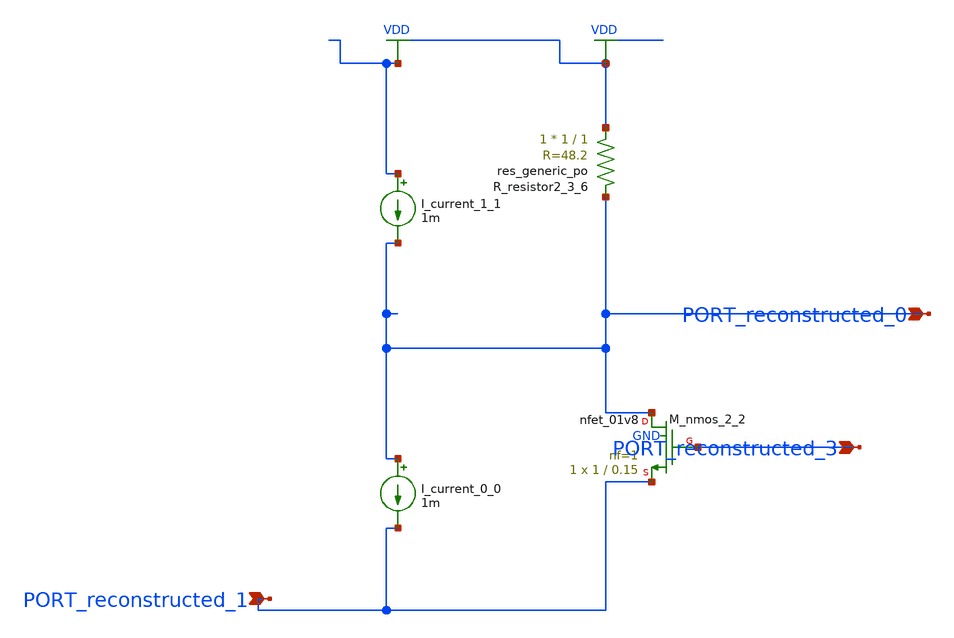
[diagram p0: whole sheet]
** sch_path: schematics/AMSNet/469.sch
**.subckt 469 PORT_reconstructed_3 PORT_reconstructed_1 PORT_reconstructed_0
*.ipin PORT_reconstructed_3
*.ipin PORT_reconstructed_1
*.ipin PORT_reconstructed_0
I_current_0_0 PORT_reconstructed_0 PORT_reconstructed_1 1m
I_current_1_1 VDD PORT_reconstructed_0 1m
XM_nmos_2_2 PORT_reconstructed_0 PORT_reconstructed_3 PORT_reconstructed_1 GND sky130_fd_pr__nfet_01v8
+ L=0.15 W=1 nf=1 ad='int((1 + 1)/2) * 1 / 1 * 0.29' as='int((1 + 2)/2) * 1 / 1 * 0.29' pd='2*int((1 + 1)/2) * (1 / 1 + 0.29)'
+ ps='2*int((1 + 2)/2) * (1 / 1 + 0.29)' nrd='0.29 / 1 ' nrs='0.29 / 1 ' sa=0 sb=0 sd=0 mult=1 m=1
XR_resistor2_3_6 VDD PORT_reconstructed_0 sky130_fd_pr__res_generic_po W=1 L=1 m=1
**.ends
.GLOBAL VDD
.end
